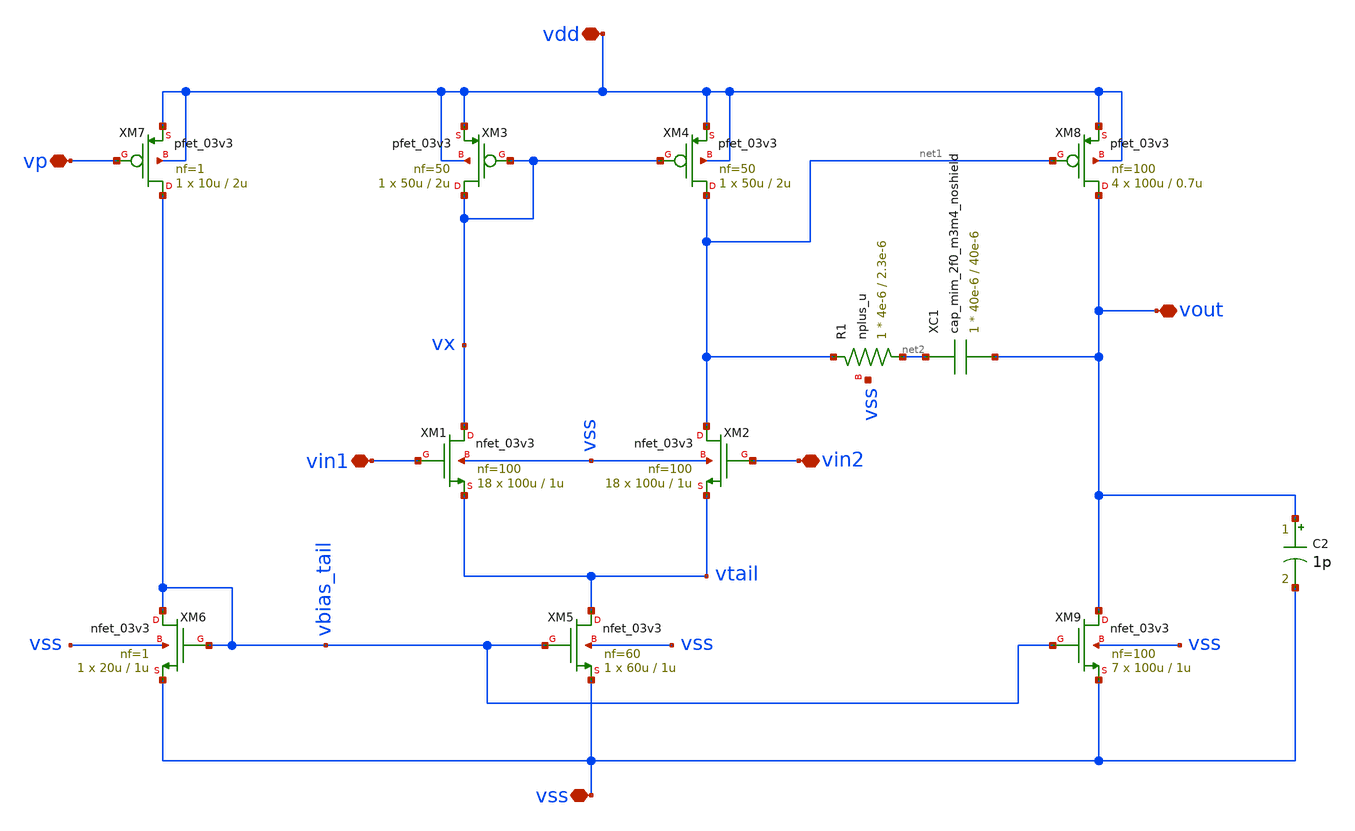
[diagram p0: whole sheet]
** sch_path: designs/comparator/preamp/2stage_opamp.sch
**.subckt 2stage_opamp vss vin1 vin2 vp vout vdd
*.iopin vss
*.iopin vin1
*.iopin vin2
*.iopin vp
*.iopin vout
*.iopin vdd
XM1 vx vin1 vtail vss nfet_03v3 L=1u W=100u nf=100 ad='int((nf+1)/2) * W/nf * 0.18u' as='int((nf+2)/2) * W/nf * 0.18u'
+ pd='2*int((nf+1)/2) * (W/nf + 0.18u)' ps='2*int((nf+2)/2) * (W/nf + 0.18u)' nrd='0.18u / W' nrs='0.18u / W'
+ sa=0 sb=0 sd=0 m=18
XM2 net1 vin2 vtail vss nfet_03v3 L=1u W=100u nf=100 ad='int((nf+1)/2) * W/nf * 0.18u' as='int((nf+2)/2) * W/nf * 0.18u'
+ pd='2*int((nf+1)/2) * (W/nf + 0.18u)' ps='2*int((nf+2)/2) * (W/nf + 0.18u)' nrd='0.18u / W' nrs='0.18u / W'
+ sa=0 sb=0 sd=0 m=18
XM3 vx vx vdd vdd pfet_03v3 L=2u W=50u nf=50 ad='int((nf+1)/2) * W/nf * 0.18u' as='int((nf+2)/2) * W/nf * 0.18u'
+ pd='2*int((nf+1)/2) * (W/nf + 0.18u)' ps='2*int((nf+2)/2) * (W/nf + 0.18u)' nrd='0.18u / W' nrs='0.18u / W'
+ sa=0 sb=0 sd=0 m=1
XM4 net1 vx vdd vdd pfet_03v3 L=2u W=50u nf=50 ad='int((nf+1)/2) * W/nf * 0.18u' as='int((nf+2)/2) * W/nf * 0.18u'
+ pd='2*int((nf+1)/2) * (W/nf + 0.18u)' ps='2*int((nf+2)/2) * (W/nf + 0.18u)' nrd='0.18u / W' nrs='0.18u / W'
+ sa=0 sb=0 sd=0 m=1
XM5 vtail vbias_tail vss vss nfet_03v3 L=1u W=60u nf=60 ad='int((nf+1)/2) * W/nf * 0.18u' as='int((nf+2)/2) * W/nf * 0.18u'
+ pd='2*int((nf+1)/2) * (W/nf + 0.18u)' ps='2*int((nf+2)/2) * (W/nf + 0.18u)' nrd='0.18u / W' nrs='0.18u / W'
+ sa=0 sb=0 sd=0 m=1
XM6 vbias_tail vbias_tail vss vss nfet_03v3 L=1u W=20u nf=1 ad='int((nf+1)/2) * W/nf * 0.18u' as='int((nf+2)/2) * W/nf * 0.18u'
+ pd='2*int((nf+1)/2) * (W/nf + 0.18u)' ps='2*int((nf+2)/2) * (W/nf + 0.18u)' nrd='0.18u / W' nrs='0.18u / W'
+ sa=0 sb=0 sd=0 m=1
XM7 vbias_tail vp vdd vdd pfet_03v3 L=2u W=10u nf=1 ad='int((nf+1)/2) * W/nf * 0.18u' as='int((nf+2)/2) * W/nf * 0.18u'
+ pd='2*int((nf+1)/2) * (W/nf + 0.18u)' ps='2*int((nf+2)/2) * (W/nf + 0.18u)' nrd='0.18u / W' nrs='0.18u / W'
+ sa=0 sb=0 sd=0 m=1
XM8 vout net1 vdd vdd pfet_03v3 L=0.7u W=100u nf=100 ad='int((nf+1)/2) * W/nf * 0.18u' as='int((nf+2)/2) * W/nf * 0.18u'
+ pd='2*int((nf+1)/2) * (W/nf + 0.18u)' ps='2*int((nf+2)/2) * (W/nf + 0.18u)' nrd='0.18u / W' nrs='0.18u / W'
+ sa=0 sb=0 sd=0 m=4
XM9 vout vbias_tail vss vss nfet_03v3 L=1u W=100u nf=100 ad='int((nf+1)/2) * W/nf * 0.18u' as='int((nf+2)/2) * W/nf * 0.18u'
+ pd='2*int((nf+1)/2) * (W/nf + 0.18u)' ps='2*int((nf+2)/2) * (W/nf + 0.18u)' nrd='0.18u / W' nrs='0.18u / W'
+ sa=0 sb=0 sd=0 m=7
XR1 net2 net1 vss nplus_u r_width=4e-6 r_length=2.3e-6 m=1
C2 vout vss 1p m=1
XC1 net2 vout cap_mim_2f0_m3m4_noshield c_width=40e-6 c_length=40e-6 m=1
**.ends
.end
